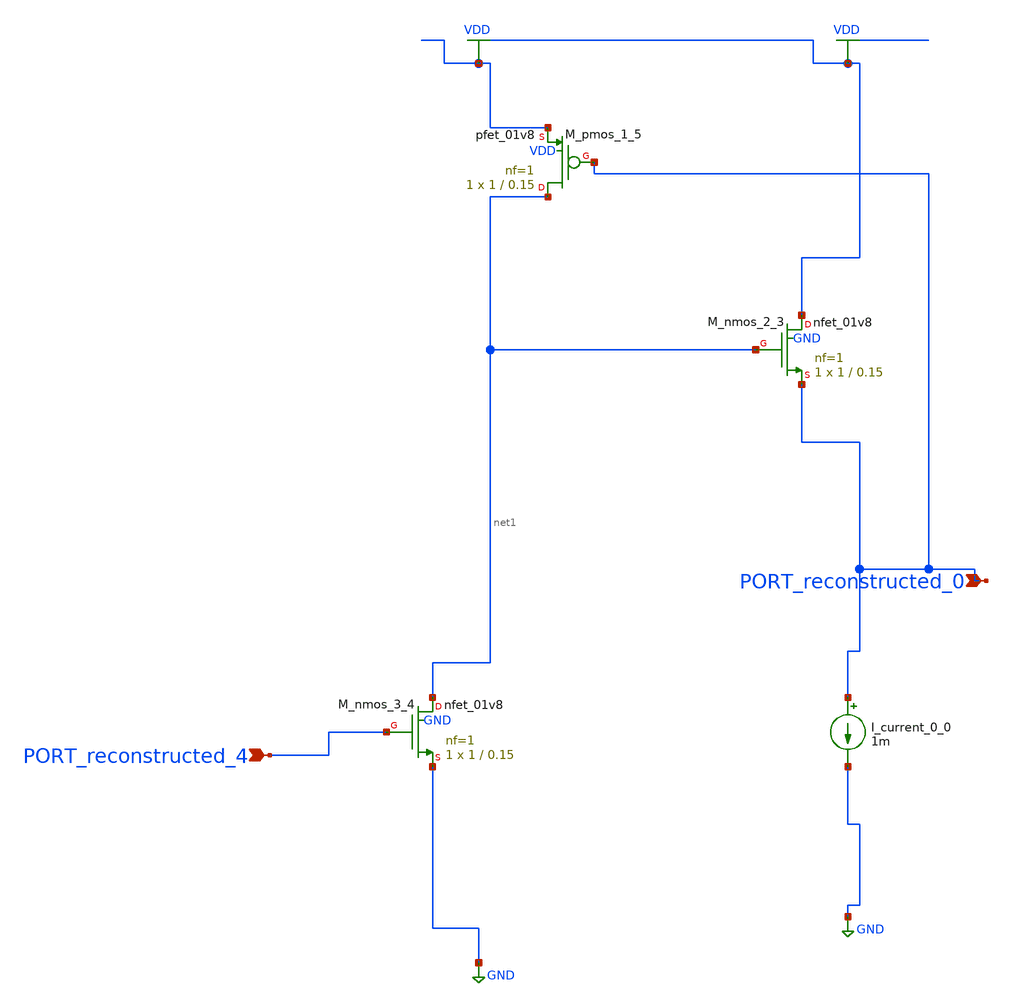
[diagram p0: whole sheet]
** sch_path: schematics/AMSNet/180.sch
**.subckt 180 PORT_reconstructed_0 PORT_reconstructed_4
*.ipin PORT_reconstructed_0
*.ipin PORT_reconstructed_4
I_current_0_0 PORT_reconstructed_0 GND 1m
XM_nmos_2_3 VDD net1 PORT_reconstructed_0 GND sky130_fd_pr__nfet_01v8 L=0.15 W=1 nf=1 ad='int((1 + 1)/2) * 1 / 1 * 0.29'
+ as='int((1 + 2)/2) * 1 / 1 * 0.29' pd='2*int((1 + 1)/2) * (1 / 1 + 0.29)' ps='2*int((1 + 2)/2) * (1 / 1 + 0.29)'
+ nrd='0.29 / 1 ' nrs='0.29 / 1 ' sa=0 sb=0 sd=0 mult=1 m=1
XM_nmos_3_4 net1 PORT_reconstructed_4 GND GND sky130_fd_pr__nfet_01v8 L=0.15 W=1 nf=1 ad='int((1 + 1)/2) * 1 / 1 * 0.29'
+ as='int((1 + 2)/2) * 1 / 1 * 0.29' pd='2*int((1 + 1)/2) * (1 / 1 + 0.29)' ps='2*int((1 + 2)/2) * (1 / 1 + 0.29)'
+ nrd='0.29 / 1 ' nrs='0.29 / 1 ' sa=0 sb=0 sd=0 mult=1 m=1
XM_pmos_1_5 net1 PORT_reconstructed_0 VDD VDD sky130_fd_pr__pfet_01v8 L=0.15 W=1 nf=1 ad='int((1 + 1)/2) * 1 / 1 * 0.29'
+ as='int((1 + 2)/2) * 1 / 1 * 0.29' pd='2*int((1 + 1)/2) * (1 / 1 + 0.29)' ps='2*int((1 + 2)/2) * (1 / 1 + 0.29)'
+ nrd='0.29 / 1 ' nrs='0.29 / 1 ' sa=0 sb=0 sd=0 mult=1 m=1
**.ends
.GLOBAL GND
.GLOBAL VDD
.end
